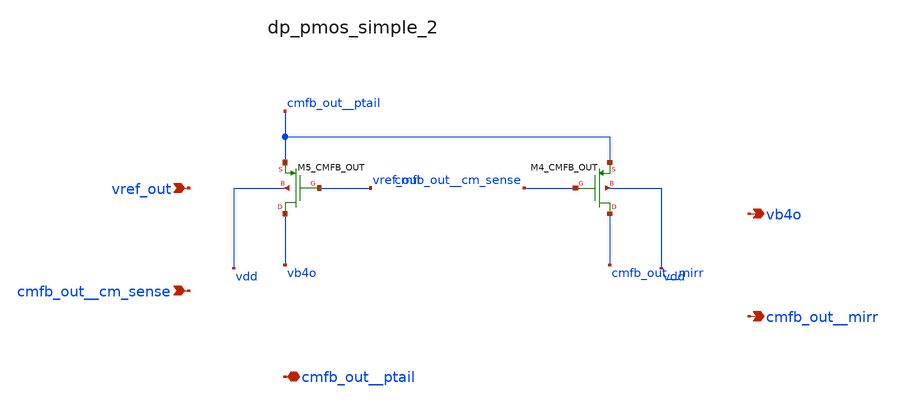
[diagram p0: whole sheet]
** sch_path: analog-db/raw/amp_035_fan_chopper_cmfb_dual/hier/blocks/dp_pmos_simple_2.sch
**.subckt dp_pmos_simple_2 vref_out cmfb_out__cm_sense cmfb_out__ptail vb4o cmfb_out__mirr
*.ipin vref_out
*.ipin cmfb_out__cm_sense
*.iopin cmfb_out__ptail
*.opin vb4o
*.opin cmfb_out__mirr
XM4_CMFB_OUT cmfb_out__mirr cmfb_out__cm_sense cmfb_out__ptail vdd sg13_lv_pmos
+ w=x_dut_xm4_cmfb_out_w l=x_dut_xm4_cmfb_out_l ng=1 m=x_dut_xm4_cmfb_out_m
XM5_CMFB_OUT vb4o vref_out cmfb_out__ptail vdd sg13_lv_pmos w=x_dut_xm5_cmfb_out_w
+ l=x_dut_xm5_cmfb_out_l ng=1 m=x_dut_xm5_cmfb_out_m
**.ends
.end
